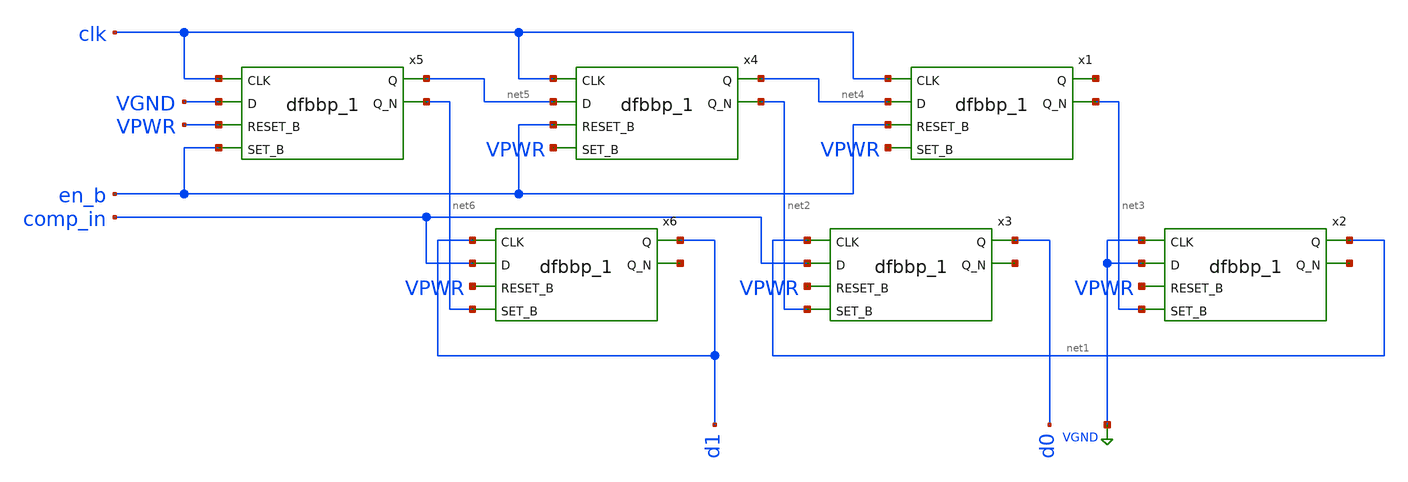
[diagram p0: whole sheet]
** sch_path: untitled-2.sch
**.subckt untitled-2
x1 clk net4 en_b VPWR VGND VNB VPB VPWR net7 net3 sky130_fd_sc_hd__dfbbp_1
x2 VGND VGND VPWR net3 VGND VNB VPB VPWR net1 net8 sky130_fd_sc_hd__dfbbp_1
x3 net1 comp_in VPWR net2 VGND VNB VPB VPWR d0 net9 sky130_fd_sc_hd__dfbbp_1
x4 clk net5 en_b VPWR VGND VNB VPB VPWR net4 net2 sky130_fd_sc_hd__dfbbp_1
x5 clk VGND VPWR en_b VGND VNB VPB VPWR net5 net6 sky130_fd_sc_hd__dfbbp_1
x6 d1 comp_in VPWR net6 VGND VNB VPB VPWR d1 net10 sky130_fd_sc_hd__dfbbp_1
**.ends
.GLOBAL VGND
.end
